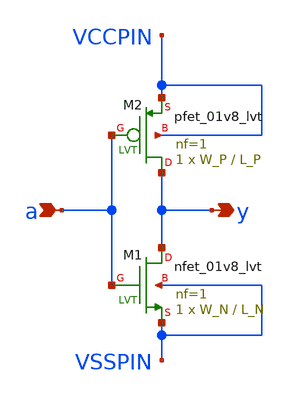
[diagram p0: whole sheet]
** sch_path: pdks/sky130A-1.0.227.01/libs.tech/xschem/sky130_tests/lvtnot.sch
* Copyright 2021 Stefan Frederik Schippers
* Licensed under the Apache License, Version 2.0 (the "License");
* you may not use this file except in compliance with the License.
* You may obtain a copy of the License at
* https://www.apache.org/licenses/LICENSE-2.0
* Unless required by applicable law or agreed to in writing, software
* distributed under the License is distributed on an "AS IS" BASIS,
* WITHOUT WARRANTIES OR CONDITIONS OF ANY KIND, either express or implied.
* See the License for the specific language governing permissions and
* limitations under the License.
**.subckt lvtnot y a
*.opin y
*.ipin a
XM2 y a VCCPIN VCCPIN sky130_fd_pr__pfet_01v8_lvt L=L_P W=W_P nf=1 ad='int((1 + 1)/2) * W_P / 1 * 0.29'
+ as='int((1 + 2)/2) * W_P / 1 * 0.29' pd='2*int((1 + 1)/2) * (W_P / 1 + 0.29)' ps='2*int((1 + 2)/2) * (W_P / 1 + 0.29)'
+ nrd='0.29 / W_P ' nrs='0.29 / W_P ' sa=0 sb=0 sd=0 mult=1 m=1
XM1 y a VSSPIN VSSPIN sky130_fd_pr__nfet_01v8_lvt L=L_N W=W_N nf=1 ad='int((1 + 1)/2) * W_N / 1 * 0.29'
+ as='int((1 + 2)/2) * W_N / 1 * 0.29' pd='2*int((1 + 1)/2) * (W_N / 1 + 0.29)' ps='2*int((1 + 2)/2) * (W_N / 1 + 0.29)'
+ nrd='0.29 / W_N ' nrs='0.29 / W_N ' sa=0 sb=0 sd=0 mult=1 m=1
**** begin user architecture code

.lib $::SKYWATER_MODELS/sky130.lib.spice tt

**** end user architecture code
**.ends
.end
